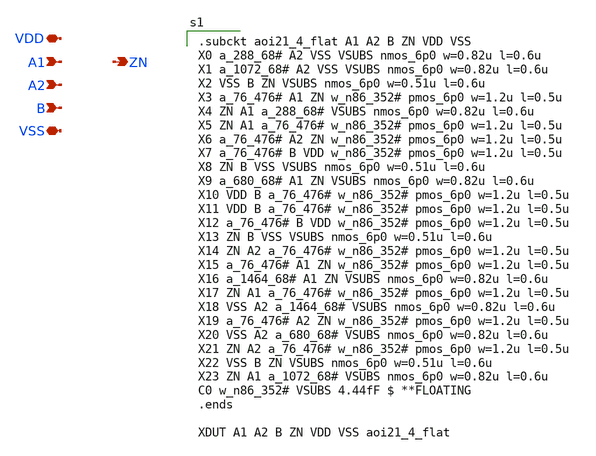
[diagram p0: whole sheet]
** sch_path: xschem/aoi21_4.sch
**.subckt aoi21_4 A1 A2 B ZN VDD VSS
*.ipin A1
*.ipin A2
*.ipin B
*.opin ZN
*.iopin VDD
*.iopin VSS
**** begin user architecture code

.subckt aoi21_4_flat A1 A2 B ZN VDD VSS
X0 a_288_68# A2 VSS VSUBS nmos_6p0 w=0.82u l=0.6u
X1 a_1072_68# A2 VSS VSUBS nmos_6p0 w=0.82u l=0.6u
X2 VSS B ZN VSUBS nmos_6p0 w=0.51u l=0.6u
X3 a_76_476# A1 ZN w_n86_352# pmos_6p0 w=1.2u l=0.5u
X4 ZN A1 a_288_68# VSUBS nmos_6p0 w=0.82u l=0.6u
X5 ZN A1 a_76_476# w_n86_352# pmos_6p0 w=1.2u l=0.5u
X6 a_76_476# A2 ZN w_n86_352# pmos_6p0 w=1.2u l=0.5u
X7 a_76_476# B VDD w_n86_352# pmos_6p0 w=1.2u l=0.5u
X8 ZN B VSS VSUBS nmos_6p0 w=0.51u l=0.6u
X9 a_680_68# A1 ZN VSUBS nmos_6p0 w=0.82u l=0.6u
X10 VDD B a_76_476# w_n86_352# pmos_6p0 w=1.2u l=0.5u
X11 VDD B a_76_476# w_n86_352# pmos_6p0 w=1.2u l=0.5u
X12 a_76_476# B VDD w_n86_352# pmos_6p0 w=1.2u l=0.5u
X13 ZN B VSS VSUBS nmos_6p0 w=0.51u l=0.6u
X14 ZN A2 a_76_476# w_n86_352# pmos_6p0 w=1.2u l=0.5u
X15 a_76_476# A1 ZN w_n86_352# pmos_6p0 w=1.2u l=0.5u
X16 a_1464_68# A1 ZN VSUBS nmos_6p0 w=0.82u l=0.6u
X17 ZN A1 a_76_476# w_n86_352# pmos_6p0 w=1.2u l=0.5u
X18 VSS A2 a_1464_68# VSUBS nmos_6p0 w=0.82u l=0.6u
X19 a_76_476# A2 ZN w_n86_352# pmos_6p0 w=1.2u l=0.5u
X20 VSS A2 a_680_68# VSUBS nmos_6p0 w=0.82u l=0.6u
X21 ZN A2 a_76_476# w_n86_352# pmos_6p0 w=1.2u l=0.5u
X22 VSS B ZN VSUBS nmos_6p0 w=0.51u l=0.6u
X23 ZN A1 a_1072_68# VSUBS nmos_6p0 w=0.82u l=0.6u
C0 w_n86_352# VSUBS 4.44fF $ **FLOATING
.ends

XDUT A1 A2 B ZN VDD VSS aoi21_4_flat


**** end user architecture code
**.ends
.end
